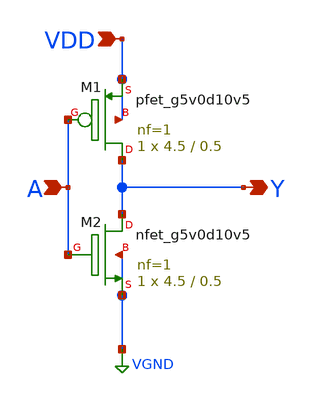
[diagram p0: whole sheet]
** sch_path: xschem/skullfet_inverter_5v_pwr.sch
**.subckt skullfet_inverter_5v_pwr A Y VDD
*.ipin A
*.opin Y
*.ipin VDD
XM1 Y A VDD VDD sky130_fd_pr__pfet_g5v0d10v5 L=0.5 W=4.5 nf=1 ad=5.3775 as=7.5825 pd=12.07 ps=29.53 nrd='0.29 / 4.5 '
+ nrs='0.29 / 4.5 ' sa=0 sb=0 sd=0 mult=1 m=1
XM2 Y A VGND VGND sky130_fd_pr__nfet_g5v0d10v5 L=0.5 W=4.5 nf=1 ad=7.8525 as=5.1075 pd=29.65 ps=11.95
+ nrd='0.29 / 4.5 ' nrs='0.29 / 4.5 ' sa=0 sb=0 sd=0 mult=1 m=1
**.ends
.GLOBAL VGND
.end
